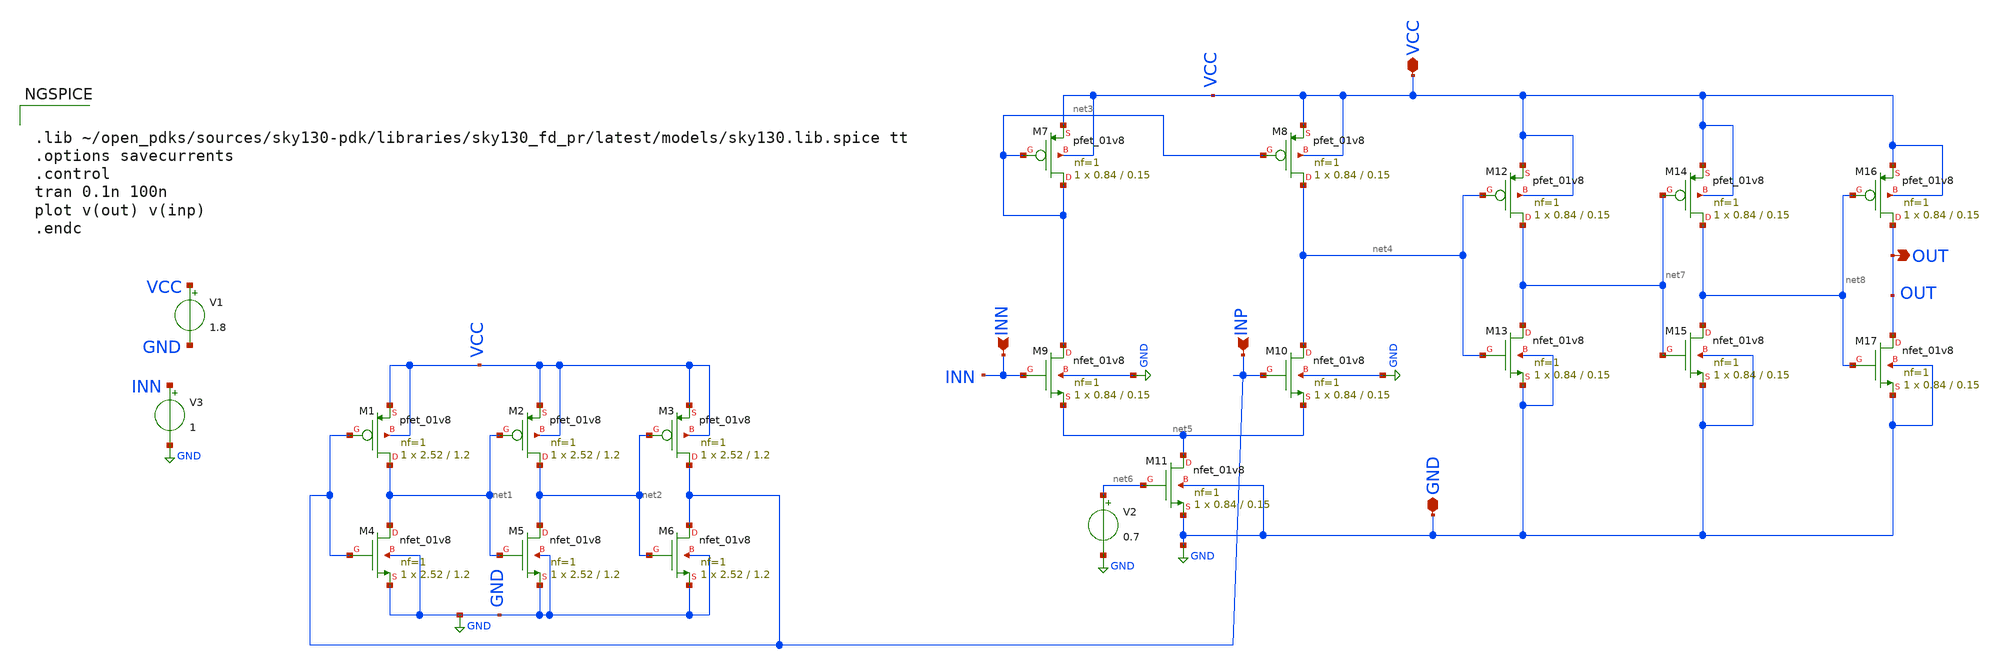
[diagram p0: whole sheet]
** sch_path: Week 4/xschem/ring_oscillator.sch
**.subckt ring_oscillator OUT VCC GND INP INN
*.opin OUT
*.iopin VCC
*.iopin GND
*.ipin INP
*.ipin INN
XM1 net1 INP VCC VCC sky130_fd_pr__pfet_01v8 L=1.2 W=2.52 nf=1 ad='int((nf+1)/2) * W/nf * 0.29' as='int((nf+2)/2) * W/nf * 0.29'
+ pd='2*int((nf+1)/2) * (W/nf + 0.29)' ps='2*int((nf+2)/2) * (W/nf + 0.29)' nrd='0.29 / W' nrs='0.29 / W'
+ sa=0 sb=0 sd=0 mult=1 m=1
XM2 net2 net1 VCC VCC sky130_fd_pr__pfet_01v8 L=1.2 W=2.52 nf=1 ad='int((nf+1)/2) * W/nf * 0.29' as='int((nf+2)/2) * W/nf * 0.29'
+ pd='2*int((nf+1)/2) * (W/nf + 0.29)' ps='2*int((nf+2)/2) * (W/nf + 0.29)' nrd='0.29 / W' nrs='0.29 / W'
+ sa=0 sb=0 sd=0 mult=1 m=1
XM3 INP net2 VCC VCC sky130_fd_pr__pfet_01v8 L=1.2 W=2.52 nf=1 ad='int((nf+1)/2) * W/nf * 0.29' as='int((nf+2)/2) * W/nf * 0.29'
+ pd='2*int((nf+1)/2) * (W/nf + 0.29)' ps='2*int((nf+2)/2) * (W/nf + 0.29)' nrd='0.29 / W' nrs='0.29 / W'
+ sa=0 sb=0 sd=0 mult=1 m=1
XM4 net1 INP GND GND sky130_fd_pr__nfet_01v8 L=1.2 W=2.52 nf=1 ad='int((nf+1)/2) * W/nf * 0.29' as='int((nf+2)/2) * W/nf * 0.29'
+ pd='2*int((nf+1)/2) * (W/nf + 0.29)' ps='2*int((nf+2)/2) * (W/nf + 0.29)' nrd='0.29 / W' nrs='0.29 / W'
+ sa=0 sb=0 sd=0 mult=1 m=1
XM5 net2 net1 GND GND sky130_fd_pr__nfet_01v8 L=1.2 W=2.52 nf=1 ad='int((nf+1)/2) * W/nf * 0.29' as='int((nf+2)/2) * W/nf * 0.29'
+ pd='2*int((nf+1)/2) * (W/nf + 0.29)' ps='2*int((nf+2)/2) * (W/nf + 0.29)' nrd='0.29 / W' nrs='0.29 / W'
+ sa=0 sb=0 sd=0 mult=1 m=1
XM6 INP net2 GND GND sky130_fd_pr__nfet_01v8 L=1.2 W=2.52 nf=1 ad='int((nf+1)/2) * W/nf * 0.29' as='int((nf+2)/2) * W/nf * 0.29'
+ pd='2*int((nf+1)/2) * (W/nf + 0.29)' ps='2*int((nf+2)/2) * (W/nf + 0.29)' nrd='0.29 / W' nrs='0.29 / W'
+ sa=0 sb=0 sd=0 mult=1 m=1
V1 VCC GND 1.8
XM7 net3 net3 VCC VCC sky130_fd_pr__pfet_01v8 L=0.15 W=0.84 nf=1 ad='int((nf+1)/2) * W/nf * 0.29' as='int((nf+2)/2) * W/nf * 0.29'
+ pd='2*int((nf+1)/2) * (W/nf + 0.29)' ps='2*int((nf+2)/2) * (W/nf + 0.29)' nrd='0.29 / W' nrs='0.29 / W'
+ sa=0 sb=0 sd=0 mult=1 m=1
XM8 net4 net3 VCC VCC sky130_fd_pr__pfet_01v8 L=0.15 W=0.84 nf=1 ad='int((nf+1)/2) * W/nf * 0.29' as='int((nf+2)/2) * W/nf * 0.29'
+ pd='2*int((nf+1)/2) * (W/nf + 0.29)' ps='2*int((nf+2)/2) * (W/nf + 0.29)' nrd='0.29 / W' nrs='0.29 / W'
+ sa=0 sb=0 sd=0 mult=1 m=1
XM9 net3 INN net5 GND sky130_fd_pr__nfet_01v8 L=0.15 W=0.84 nf=1 ad='int((nf+1)/2) * W/nf * 0.29' as='int((nf+2)/2) * W/nf * 0.29'
+ pd='2*int((nf+1)/2) * (W/nf + 0.29)' ps='2*int((nf+2)/2) * (W/nf + 0.29)' nrd='0.29 / W' nrs='0.29 / W'
+ sa=0 sb=0 sd=0 mult=1 m=1
XM10 net4 INP net5 GND sky130_fd_pr__nfet_01v8 L=0.15 W=0.84 nf=1 ad='int((nf+1)/2) * W/nf * 0.29' as='int((nf+2)/2) * W/nf * 0.29'
+ pd='2*int((nf+1)/2) * (W/nf + 0.29)' ps='2*int((nf+2)/2) * (W/nf + 0.29)' nrd='0.29 / W' nrs='0.29 / W'
+ sa=0 sb=0 sd=0 mult=1 m=1
XM11 net5 net6 GND GND sky130_fd_pr__nfet_01v8 L=0.15 W=0.84 nf=1 ad='int((nf+1)/2) * W/nf * 0.29' as='int((nf+2)/2) * W/nf * 0.29'
+ pd='2*int((nf+1)/2) * (W/nf + 0.29)' ps='2*int((nf+2)/2) * (W/nf + 0.29)' nrd='0.29 / W' nrs='0.29 / W'
+ sa=0 sb=0 sd=0 mult=1 m=1
V2 net6 GND 0.7
XM12 net7 net4 VCC VCC sky130_fd_pr__pfet_01v8 L=0.15 W=0.84 nf=1 ad='int((nf+1)/2) * W/nf * 0.29' as='int((nf+2)/2) * W/nf * 0.29'
+ pd='2*int((nf+1)/2) * (W/nf + 0.29)' ps='2*int((nf+2)/2) * (W/nf + 0.29)' nrd='0.29 / W' nrs='0.29 / W'
+ sa=0 sb=0 sd=0 mult=1 m=1
XM13 net7 net4 GND GND sky130_fd_pr__nfet_01v8 L=0.15 W=0.84 nf=1 ad='int((nf+1)/2) * W/nf * 0.29' as='int((nf+2)/2) * W/nf * 0.29'
+ pd='2*int((nf+1)/2) * (W/nf + 0.29)' ps='2*int((nf+2)/2) * (W/nf + 0.29)' nrd='0.29 / W' nrs='0.29 / W'
+ sa=0 sb=0 sd=0 mult=1 m=1
XM14 net8 net7 VCC VCC sky130_fd_pr__pfet_01v8 L=0.15 W=0.84 nf=1 ad='int((nf+1)/2) * W/nf * 0.29' as='int((nf+2)/2) * W/nf * 0.29'
+ pd='2*int((nf+1)/2) * (W/nf + 0.29)' ps='2*int((nf+2)/2) * (W/nf + 0.29)' nrd='0.29 / W' nrs='0.29 / W'
+ sa=0 sb=0 sd=0 mult=1 m=1
XM15 net8 net7 GND GND sky130_fd_pr__nfet_01v8 L=0.15 W=0.84 nf=1 ad='int((nf+1)/2) * W/nf * 0.29' as='int((nf+2)/2) * W/nf * 0.29'
+ pd='2*int((nf+1)/2) * (W/nf + 0.29)' ps='2*int((nf+2)/2) * (W/nf + 0.29)' nrd='0.29 / W' nrs='0.29 / W'
+ sa=0 sb=0 sd=0 mult=1 m=1
XM16 OUT net8 VCC VCC sky130_fd_pr__pfet_01v8 L=0.15 W=0.84 nf=1 ad='int((nf+1)/2) * W/nf * 0.29' as='int((nf+2)/2) * W/nf * 0.29'
+ pd='2*int((nf+1)/2) * (W/nf + 0.29)' ps='2*int((nf+2)/2) * (W/nf + 0.29)' nrd='0.29 / W' nrs='0.29 / W'
+ sa=0 sb=0 sd=0 mult=1 m=1
XM17 OUT net8 GND GND sky130_fd_pr__nfet_01v8 L=0.15 W=0.84 nf=1 ad='int((nf+1)/2) * W/nf * 0.29' as='int((nf+2)/2) * W/nf * 0.29'
+ pd='2*int((nf+1)/2) * (W/nf + 0.29)' ps='2*int((nf+2)/2) * (W/nf + 0.29)' nrd='0.29 / W' nrs='0.29 / W'
+ sa=0 sb=0 sd=0 mult=1 m=1
V3 INN GND 1
**** begin user architecture code


.lib ~/open_pdks/sources/sky130-pdk/libraries/sky130_fd_pr/latest/models/sky130.lib.spice tt
.options savecurrents
.control
tran 0.1n 100n
plot v(out) v(inp)
.endc


**** end user architecture code
**.ends
.GLOBAL GND
.end
